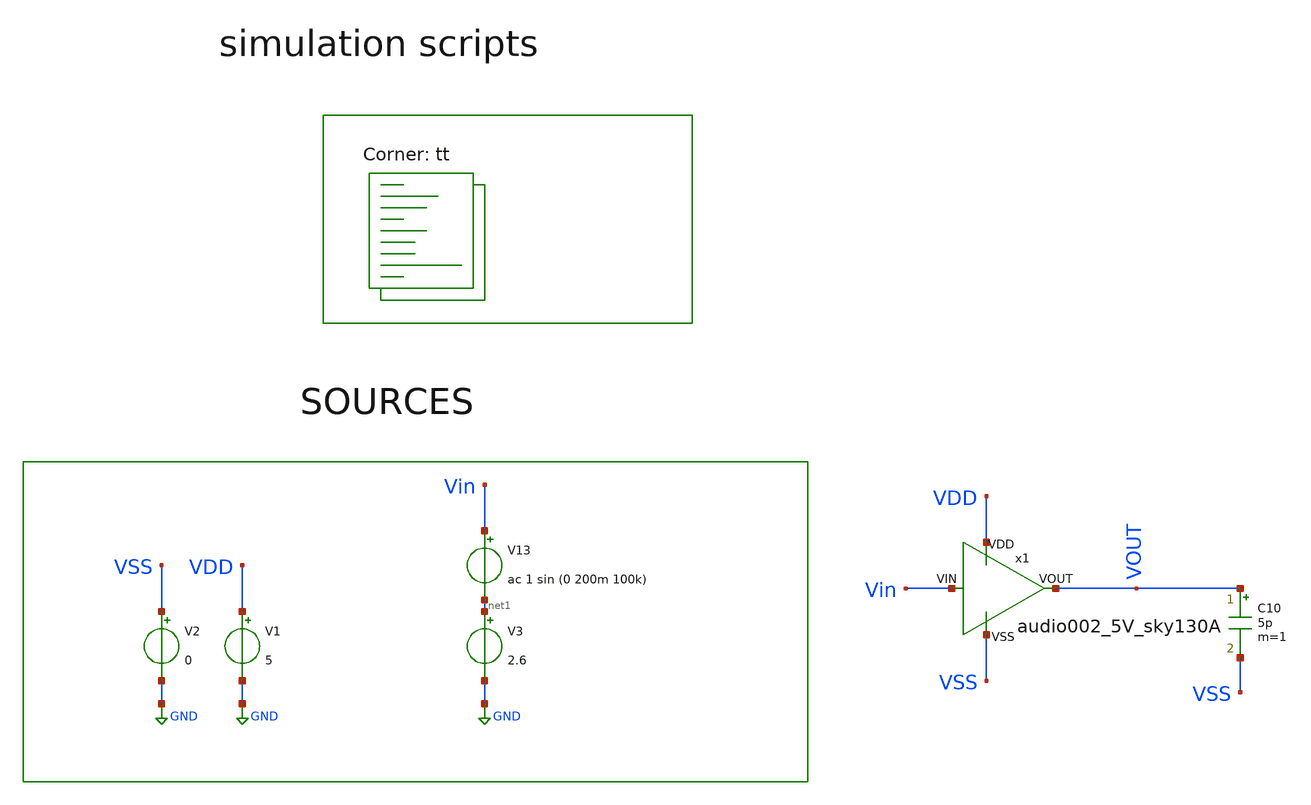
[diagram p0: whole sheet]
** sch_path: my_ip/sky130A/primordial_bicmos_tb/tb.sch
**.subckt tb
V1 VDD GND 5
V2 VSS GND 0
V3 net1 GND 2.6
C10 VOUT VSS 5p m=1
V13 Vin net1 ac 1 sin (0 200m 100k)
x1 VDD VSS Vin VOUT audio002_5V_sky130A
**** begin user architecture code
.lib $::SKYWATER_MODELS/sky130.lib.spice tt

**************************************************************
**************************************************************
**************************************************************
**************************************************************
**************************************************************
*LIBs*********************************************************
**************************************************************
**************************************************************
**************************************************************
**************************************************************
**************************************************************
*.lib $::SKYWATER_MODELS/sky130.lib.spice tt
* chose the corners in the corner file
* tt_mm for mismatch
* ss ff sf fs standart corners
* ll hh lh hl capacitor and resistors corners
* mc for total process variation including corners
**************************************************************
**************************************************************
**************************************************************
**************************************************************
**************************************************************
*Corners/montecarlo options***********************************
**************************************************************
**************************************************************
**************************************************************
**************************************************************
**************************************************************
.TEMP 27
**************************************************************
**************************************************************
**************************************************************
**************************************************************
*SIMULATION and Plots*****************************************
**************************************************************
**************************************************************
**************************************************************
**************************************************************
.include ~/PDK/sky130A/libs.ref/sky130_fd_sc_hd/spice/sky130_fd_sc_hd.spice



.control
save all
op
write tb.raw
set appendwrite

dc V3 0 5 0.001
plot v(VOUT)
ac dec 10 1 50G
plot db(v(VOUT))

tran 10ns 50u
plot v(VOUT)

set appendwrite
write tb.raw

.endc

**** end user architecture code
**.ends

* expanding   symbol:  primordial_bicmos/audio002_5V_sky130A.sym # of pins=4
** sym_path: my_ip/LIB/primordial_bicmos/audio002_5V_sky130A.sym
** sch_path: my_ip/LIB/primordial_bicmos/audio002_5V_sky130A.sch
.subckt audio002_5V_sky130A VDD VSS VIN VOUT
*.iopin VDD
*.iopin VSS
*.iopin VIN
*.iopin VOUT
XQ2 VDD net1 net2 VSS sky130_fd_pr__npn_05v5_w1p00l2p00
XQ1 VDD net2 net3 VSS sky130_fd_pr__npn_05v5_w1p00l2p00
XQ3 VOUT net3 net4 VSS sky130_fd_pr__npn_05v5_w1p00l2p00
R1 net4 VSS 100 m=1
R2 VDD VOUT 1k m=1
XM2 net1 VIN VDD VDD sky130_fd_pr__pfet_g5v0d10v5 L=0.5 W='4 * 4 ' nf=4 ad='int((4 + 1)/2) * 4 * 0.29'
+ as='int((4 + 2)/2) * 4 * 0.29' pd='2*int((4 + 1)/2) * (4 + 0.29)' ps='2*int((4 + 2)/2) * (4 + 0.29)'
+ nrd='0.29 / 4 / 4 ' nrs='0.29 / 4 / 4 ' sa=0 sb=0 sd=0 mult=4 m=4
XM1 VSS VSS net1 VDD sky130_fd_pr__pfet_g5v0d10v5 L=0.5 W='3 * 4 ' nf=4 ad='int((4 + 1)/2) * 3 * 0.29'
+ as='int((4 + 2)/2) * 3 * 0.29' pd='2*int((4 + 1)/2) * (3 + 0.29)' ps='2*int((4 + 2)/2) * (3 + 0.29)'
+ nrd='0.29 / 3 / 4 ' nrs='0.29 / 3 / 4 ' sa=0 sb=0 sd=0 mult=4 m=4
.ends

.GLOBAL GND
.end
